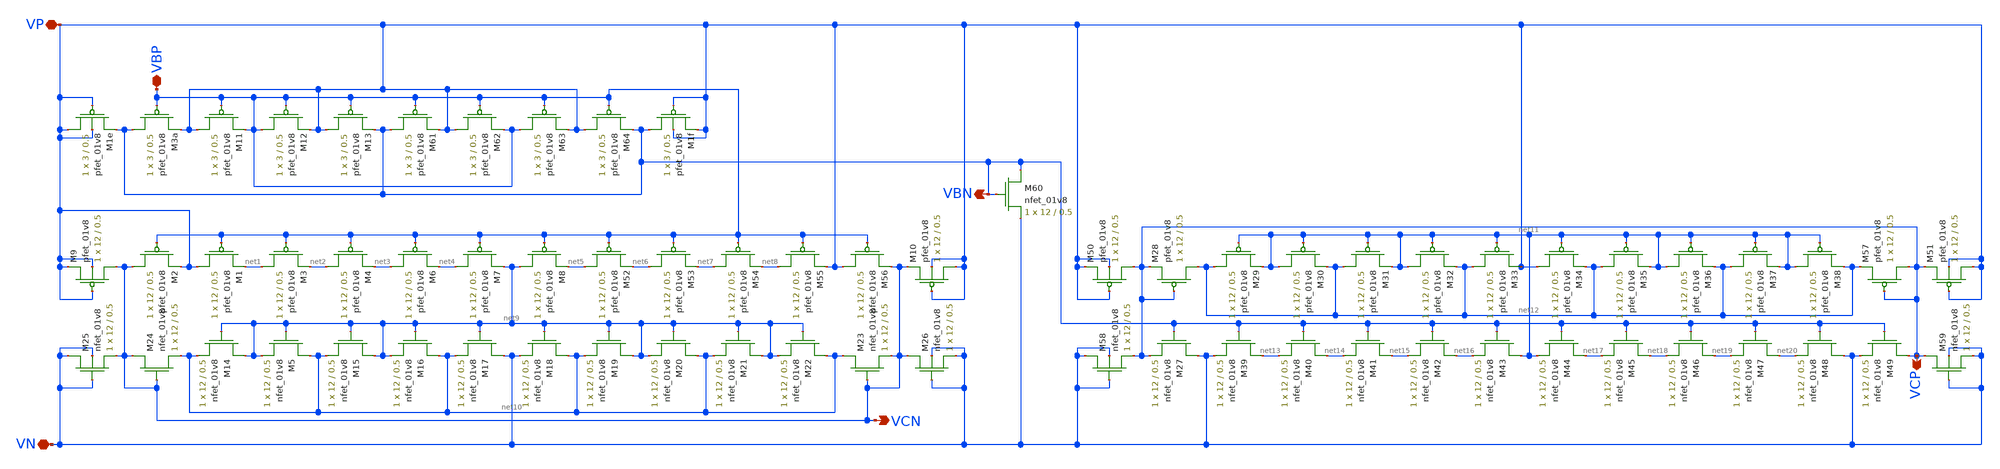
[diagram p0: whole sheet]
** sch_path: differential_amplifier/schematics/bias_generator.sch
**.subckt bias_generator VBP VP VN VCN VCP VBN
*.iopin VBP
*.iopin VP
*.iopin VN
*.opin VCN
*.opin VCP
*.opin VBN
XM9 VCN VP VP VP sky130_fd_pr__pfet_01v8 L=0.5 W=12 nf=1 ad='int((nf+1)/2) * W/nf * 0.29' as='int((nf+2)/2) * W/nf * 0.29'
+ pd='2*int((nf+1)/2) * (W/nf + 0.29)' ps='2*int((nf+2)/2) * (W/nf + 0.29)' nrd='0.29 / W' nrs='0.29 / W'
+ sa=0 sb=0 sd=0 mult=1 m=1
XM24 VCN VCN net10 VN sky130_fd_pr__nfet_01v8 L=0.5 W=12 nf=1 ad='int((nf+1)/2) * W/nf * 0.29' as='int((nf+2)/2) * W/nf * 0.29'
+ pd='2*int((nf+1)/2) * (W/nf + 0.29)' ps='2*int((nf+2)/2) * (W/nf + 0.29)' nrd='0.29 / W' nrs='0.29 / W'
+ sa=0 sb=0 sd=0 mult=1 m=1
XM2 VCN VBP VP VP sky130_fd_pr__pfet_01v8 L=0.5 W=12 nf=1 ad='int((nf+1)/2) * W/nf * 0.29' as='int((nf+2)/2) * W/nf * 0.29'
+ pd='2*int((nf+1)/2) * (W/nf + 0.29)' ps='2*int((nf+2)/2) * (W/nf + 0.29)' nrd='0.29 / W' nrs='0.29 / W'
+ sa=0 sb=0 sd=0 mult=1 m=1
XM10 VP VP VCN VP sky130_fd_pr__pfet_01v8 L=0.5 W=12 nf=1 ad='int((nf+1)/2) * W/nf * 0.29' as='int((nf+2)/2) * W/nf * 0.29'
+ pd='2*int((nf+1)/2) * (W/nf + 0.29)' ps='2*int((nf+2)/2) * (W/nf + 0.29)' nrd='0.29 / W' nrs='0.29 / W'
+ sa=0 sb=0 sd=0 mult=1 m=1
XM25 VN VN VCN VN sky130_fd_pr__nfet_01v8 L=0.5 W=12 nf=1 ad='int((nf+1)/2) * W/nf * 0.29' as='int((nf+2)/2) * W/nf * 0.29'
+ pd='2*int((nf+1)/2) * (W/nf + 0.29)' ps='2*int((nf+2)/2) * (W/nf + 0.29)' nrd='0.29 / W' nrs='0.29 / W'
+ sa=0 sb=0 sd=0 mult=1 m=1
XM26 VCN VN VN VN sky130_fd_pr__nfet_01v8 L=0.5 W=12 nf=1 ad='int((nf+1)/2) * W/nf * 0.29' as='int((nf+2)/2) * W/nf * 0.29'
+ pd='2*int((nf+1)/2) * (W/nf + 0.29)' ps='2*int((nf+2)/2) * (W/nf + 0.29)' nrd='0.29 / W' nrs='0.29 / W'
+ sa=0 sb=0 sd=0 mult=1 m=1
XM50 VCP VP VP VP sky130_fd_pr__pfet_01v8 L=0.5 W=12 nf=1 ad='int((nf+1)/2) * W/nf * 0.29' as='int((nf+2)/2) * W/nf * 0.29'
+ pd='2*int((nf+1)/2) * (W/nf + 0.29)' ps='2*int((nf+2)/2) * (W/nf + 0.29)' nrd='0.29 / W' nrs='0.29 / W'
+ sa=0 sb=0 sd=0 mult=1 m=1
XM51 VP VP VCP VP sky130_fd_pr__pfet_01v8 L=0.5 W=12 nf=1 ad='int((nf+1)/2) * W/nf * 0.29' as='int((nf+2)/2) * W/nf * 0.29'
+ pd='2*int((nf+1)/2) * (W/nf + 0.29)' ps='2*int((nf+2)/2) * (W/nf + 0.29)' nrd='0.29 / W' nrs='0.29 / W'
+ sa=0 sb=0 sd=0 mult=1 m=1
XM58 VN VN VCP VN sky130_fd_pr__nfet_01v8 L=0.5 W=12 nf=1 ad='int((nf+1)/2) * W/nf * 0.29' as='int((nf+2)/2) * W/nf * 0.29'
+ pd='2*int((nf+1)/2) * (W/nf + 0.29)' ps='2*int((nf+2)/2) * (W/nf + 0.29)' nrd='0.29 / W' nrs='0.29 / W'
+ sa=0 sb=0 sd=0 mult=1 m=1
XM59 VCP VN VN VN sky130_fd_pr__nfet_01v8 L=0.5 W=12 nf=1 ad='int((nf+1)/2) * W/nf * 0.29' as='int((nf+2)/2) * W/nf * 0.29'
+ pd='2*int((nf+1)/2) * (W/nf + 0.29)' ps='2*int((nf+2)/2) * (W/nf + 0.29)' nrd='0.29 / W' nrs='0.29 / W'
+ sa=0 sb=0 sd=0 mult=1 m=1
XM3a VBN VBP VP VP sky130_fd_pr__pfet_01v8 L=0.5 W=3 nf=1 ad='int((nf+1)/2) * W/nf * 0.29' as='int((nf+2)/2) * W/nf * 0.29'
+ pd='2*int((nf+1)/2) * (W/nf + 0.29)' ps='2*int((nf+2)/2) * (W/nf + 0.29)' nrd='0.29 / W' nrs='0.29 / W'
+ sa=0 sb=0 sd=0 mult=1 m=1
XM1e VP VP VBN VP sky130_fd_pr__pfet_01v8 L=0.5 W=3 nf=1 ad='int((nf+1)/2) * W/nf * 0.29' as='int((nf+2)/2) * W/nf * 0.29'
+ pd='2*int((nf+1)/2) * (W/nf + 0.29)' ps='2*int((nf+2)/2) * (W/nf + 0.29)' nrd='0.29 / W' nrs='0.29 / W'
+ sa=0 sb=0 sd=0 mult=1 m=1
XM1f VBN VP VP VP sky130_fd_pr__pfet_01v8 L=0.5 W=3 nf=1 ad='int((nf+1)/2) * W/nf * 0.29' as='int((nf+2)/2) * W/nf * 0.29'
+ pd='2*int((nf+1)/2) * (W/nf + 0.29)' ps='2*int((nf+2)/2) * (W/nf + 0.29)' nrd='0.29 / W' nrs='0.29 / W'
+ sa=0 sb=0 sd=0 mult=1 m=1
XM60 VBN VBN VN VN sky130_fd_pr__nfet_01v8 L=0.5 W=12 nf=1 ad='int((nf+1)/2) * W/nf * 0.29' as='int((nf+2)/2) * W/nf * 0.29'
+ pd='2*int((nf+1)/2) * (W/nf + 0.29)' ps='2*int((nf+2)/2) * (W/nf + 0.29)' nrd='0.29 / W' nrs='0.29 / W'
+ sa=0 sb=0 sd=0 mult=1 m=1
XM11 VP VBP VBP VP sky130_fd_pr__pfet_01v8 L=0.5 W=3 nf=1 ad='int((nf+1)/2) * W/nf * 0.29' as='int((nf+2)/2) * W/nf * 0.29'
+ pd='2*int((nf+1)/2) * (W/nf + 0.29)' ps='2*int((nf+2)/2) * (W/nf + 0.29)' nrd='0.29 / W' nrs='0.29 / W'
+ sa=0 sb=0 sd=0 mult=1 m=1
XM12 VBP VBP VP VP sky130_fd_pr__pfet_01v8 L=0.5 W=3 nf=1 ad='int((nf+1)/2) * W/nf * 0.29' as='int((nf+2)/2) * W/nf * 0.29'
+ pd='2*int((nf+1)/2) * (W/nf + 0.29)' ps='2*int((nf+2)/2) * (W/nf + 0.29)' nrd='0.29 / W' nrs='0.29 / W'
+ sa=0 sb=0 sd=0 mult=1 m=1
XM13 VP VBP VBN VP sky130_fd_pr__pfet_01v8 L=0.5 W=3 nf=1 ad='int((nf+1)/2) * W/nf * 0.29' as='int((nf+2)/2) * W/nf * 0.29'
+ pd='2*int((nf+1)/2) * (W/nf + 0.29)' ps='2*int((nf+2)/2) * (W/nf + 0.29)' nrd='0.29 / W' nrs='0.29 / W'
+ sa=0 sb=0 sd=0 mult=1 m=1
XM61 VBN VBP VP VP sky130_fd_pr__pfet_01v8 L=0.5 W=3 nf=1 ad='int((nf+1)/2) * W/nf * 0.29' as='int((nf+2)/2) * W/nf * 0.29'
+ pd='2*int((nf+1)/2) * (W/nf + 0.29)' ps='2*int((nf+2)/2) * (W/nf + 0.29)' nrd='0.29 / W' nrs='0.29 / W'
+ sa=0 sb=0 sd=0 mult=1 m=1
XM62 VP VBP VBP VP sky130_fd_pr__pfet_01v8 L=0.5 W=3 nf=1 ad='int((nf+1)/2) * W/nf * 0.29' as='int((nf+2)/2) * W/nf * 0.29'
+ pd='2*int((nf+1)/2) * (W/nf + 0.29)' ps='2*int((nf+2)/2) * (W/nf + 0.29)' nrd='0.29 / W' nrs='0.29 / W'
+ sa=0 sb=0 sd=0 mult=1 m=1
XM63 VBP VBP VP VP sky130_fd_pr__pfet_01v8 L=0.5 W=3 nf=1 ad='int((nf+1)/2) * W/nf * 0.29' as='int((nf+2)/2) * W/nf * 0.29'
+ pd='2*int((nf+1)/2) * (W/nf + 0.29)' ps='2*int((nf+2)/2) * (W/nf + 0.29)' nrd='0.29 / W' nrs='0.29 / W'
+ sa=0 sb=0 sd=0 mult=1 m=1
XM64 VP VBP VBN VP sky130_fd_pr__pfet_01v8 L=0.5 W=3 nf=1 ad='int((nf+1)/2) * W/nf * 0.29' as='int((nf+2)/2) * W/nf * 0.29'
+ pd='2*int((nf+1)/2) * (W/nf + 0.29)' ps='2*int((nf+2)/2) * (W/nf + 0.29)' nrd='0.29 / W' nrs='0.29 / W'
+ sa=0 sb=0 sd=0 mult=1 m=1
XM1 VP VBP net1 VP sky130_fd_pr__pfet_01v8 L=0.5 W=12 nf=1 ad='int((nf+1)/2) * W/nf * 0.29' as='int((nf+2)/2) * W/nf * 0.29'
+ pd='2*int((nf+1)/2) * (W/nf + 0.29)' ps='2*int((nf+2)/2) * (W/nf + 0.29)' nrd='0.29 / W' nrs='0.29 / W'
+ sa=0 sb=0 sd=0 mult=1 m=1
XM3 net1 VBP net2 VP sky130_fd_pr__pfet_01v8 L=0.5 W=12 nf=1 ad='int((nf+1)/2) * W/nf * 0.29' as='int((nf+2)/2) * W/nf * 0.29'
+ pd='2*int((nf+1)/2) * (W/nf + 0.29)' ps='2*int((nf+2)/2) * (W/nf + 0.29)' nrd='0.29 / W' nrs='0.29 / W'
+ sa=0 sb=0 sd=0 mult=1 m=1
XM4 net2 VBP net3 VP sky130_fd_pr__pfet_01v8 L=0.5 W=12 nf=1 ad='int((nf+1)/2) * W/nf * 0.29' as='int((nf+2)/2) * W/nf * 0.29'
+ pd='2*int((nf+1)/2) * (W/nf + 0.29)' ps='2*int((nf+2)/2) * (W/nf + 0.29)' nrd='0.29 / W' nrs='0.29 / W'
+ sa=0 sb=0 sd=0 mult=1 m=1
XM6 net3 VBP net4 VP sky130_fd_pr__pfet_01v8 L=0.5 W=12 nf=1 ad='int((nf+1)/2) * W/nf * 0.29' as='int((nf+2)/2) * W/nf * 0.29'
+ pd='2*int((nf+1)/2) * (W/nf + 0.29)' ps='2*int((nf+2)/2) * (W/nf + 0.29)' nrd='0.29 / W' nrs='0.29 / W'
+ sa=0 sb=0 sd=0 mult=1 m=1
XM7 net4 VBP net9 VP sky130_fd_pr__pfet_01v8 L=0.5 W=12 nf=1 ad='int((nf+1)/2) * W/nf * 0.29' as='int((nf+2)/2) * W/nf * 0.29'
+ pd='2*int((nf+1)/2) * (W/nf + 0.29)' ps='2*int((nf+2)/2) * (W/nf + 0.29)' nrd='0.29 / W' nrs='0.29 / W'
+ sa=0 sb=0 sd=0 mult=1 m=1
XM8 net9 VBP net5 VP sky130_fd_pr__pfet_01v8 L=0.5 W=12 nf=1 ad='int((nf+1)/2) * W/nf * 0.29' as='int((nf+2)/2) * W/nf * 0.29'
+ pd='2*int((nf+1)/2) * (W/nf + 0.29)' ps='2*int((nf+2)/2) * (W/nf + 0.29)' nrd='0.29 / W' nrs='0.29 / W'
+ sa=0 sb=0 sd=0 mult=1 m=1
XM52 net5 VBP net6 VP sky130_fd_pr__pfet_01v8 L=0.5 W=12 nf=1 ad='int((nf+1)/2) * W/nf * 0.29' as='int((nf+2)/2) * W/nf * 0.29'
+ pd='2*int((nf+1)/2) * (W/nf + 0.29)' ps='2*int((nf+2)/2) * (W/nf + 0.29)' nrd='0.29 / W' nrs='0.29 / W'
+ sa=0 sb=0 sd=0 mult=1 m=1
XM53 net6 VBP net7 VP sky130_fd_pr__pfet_01v8 L=0.5 W=12 nf=1 ad='int((nf+1)/2) * W/nf * 0.29' as='int((nf+2)/2) * W/nf * 0.29'
+ pd='2*int((nf+1)/2) * (W/nf + 0.29)' ps='2*int((nf+2)/2) * (W/nf + 0.29)' nrd='0.29 / W' nrs='0.29 / W'
+ sa=0 sb=0 sd=0 mult=1 m=1
XM54 net7 VBP net8 VP sky130_fd_pr__pfet_01v8 L=0.5 W=12 nf=1 ad='int((nf+1)/2) * W/nf * 0.29' as='int((nf+2)/2) * W/nf * 0.29'
+ pd='2*int((nf+1)/2) * (W/nf + 0.29)' ps='2*int((nf+2)/2) * (W/nf + 0.29)' nrd='0.29 / W' nrs='0.29 / W'
+ sa=0 sb=0 sd=0 mult=1 m=1
XM55 net8 VBP VP VP sky130_fd_pr__pfet_01v8 L=0.5 W=12 nf=1 ad='int((nf+1)/2) * W/nf * 0.29' as='int((nf+2)/2) * W/nf * 0.29'
+ pd='2*int((nf+1)/2) * (W/nf + 0.29)' ps='2*int((nf+2)/2) * (W/nf + 0.29)' nrd='0.29 / W' nrs='0.29 / W'
+ sa=0 sb=0 sd=0 mult=1 m=1
XM56 VP VBP VCN VP sky130_fd_pr__pfet_01v8 L=0.5 W=12 nf=1 ad='int((nf+1)/2) * W/nf * 0.29' as='int((nf+2)/2) * W/nf * 0.29'
+ pd='2*int((nf+1)/2) * (W/nf + 0.29)' ps='2*int((nf+2)/2) * (W/nf + 0.29)' nrd='0.29 / W' nrs='0.29 / W'
+ sa=0 sb=0 sd=0 mult=1 m=1
XM14 net9 net9 net10 VN sky130_fd_pr__nfet_01v8 L=0.5 W=12 nf=1 ad='int((nf+1)/2) * W/nf * 0.29' as='int((nf+2)/2) * W/nf * 0.29'
+ pd='2*int((nf+1)/2) * (W/nf + 0.29)' ps='2*int((nf+2)/2) * (W/nf + 0.29)' nrd='0.29 / W' nrs='0.29 / W'
+ sa=0 sb=0 sd=0 mult=1 m=1
XM5 net10 net9 net9 VN sky130_fd_pr__nfet_01v8 L=0.5 W=12 nf=1 ad='int((nf+1)/2) * W/nf * 0.29' as='int((nf+2)/2) * W/nf * 0.29'
+ pd='2*int((nf+1)/2) * (W/nf + 0.29)' ps='2*int((nf+2)/2) * (W/nf + 0.29)' nrd='0.29 / W' nrs='0.29 / W'
+ sa=0 sb=0 sd=0 mult=1 m=1
XM15 net9 net9 net10 VN sky130_fd_pr__nfet_01v8 L=0.5 W=12 nf=1 ad='int((nf+1)/2) * W/nf * 0.29' as='int((nf+2)/2) * W/nf * 0.29'
+ pd='2*int((nf+1)/2) * (W/nf + 0.29)' ps='2*int((nf+2)/2) * (W/nf + 0.29)' nrd='0.29 / W' nrs='0.29 / W'
+ sa=0 sb=0 sd=0 mult=1 m=1
XM16 net10 net9 net9 VN sky130_fd_pr__nfet_01v8 L=0.5 W=12 nf=1 ad='int((nf+1)/2) * W/nf * 0.29' as='int((nf+2)/2) * W/nf * 0.29'
+ pd='2*int((nf+1)/2) * (W/nf + 0.29)' ps='2*int((nf+2)/2) * (W/nf + 0.29)' nrd='0.29 / W' nrs='0.29 / W'
+ sa=0 sb=0 sd=0 mult=1 m=1
XM17 VN net9 net10 VN sky130_fd_pr__nfet_01v8 L=0.5 W=12 nf=1 ad='int((nf+1)/2) * W/nf * 0.29' as='int((nf+2)/2) * W/nf * 0.29'
+ pd='2*int((nf+1)/2) * (W/nf + 0.29)' ps='2*int((nf+2)/2) * (W/nf + 0.29)' nrd='0.29 / W' nrs='0.29 / W'
+ sa=0 sb=0 sd=0 mult=1 m=1
XM18 net10 net9 VN VN sky130_fd_pr__nfet_01v8 L=0.5 W=12 nf=1 ad='int((nf+1)/2) * W/nf * 0.29' as='int((nf+2)/2) * W/nf * 0.29'
+ pd='2*int((nf+1)/2) * (W/nf + 0.29)' ps='2*int((nf+2)/2) * (W/nf + 0.29)' nrd='0.29 / W' nrs='0.29 / W'
+ sa=0 sb=0 sd=0 mult=1 m=1
XM19 net9 net9 net10 VN sky130_fd_pr__nfet_01v8 L=0.5 W=12 nf=1 ad='int((nf+1)/2) * W/nf * 0.29' as='int((nf+2)/2) * W/nf * 0.29'
+ pd='2*int((nf+1)/2) * (W/nf + 0.29)' ps='2*int((nf+2)/2) * (W/nf + 0.29)' nrd='0.29 / W' nrs='0.29 / W'
+ sa=0 sb=0 sd=0 mult=1 m=1
XM20 net10 net9 net9 VN sky130_fd_pr__nfet_01v8 L=0.5 W=12 nf=1 ad='int((nf+1)/2) * W/nf * 0.29' as='int((nf+2)/2) * W/nf * 0.29'
+ pd='2*int((nf+1)/2) * (W/nf + 0.29)' ps='2*int((nf+2)/2) * (W/nf + 0.29)' nrd='0.29 / W' nrs='0.29 / W'
+ sa=0 sb=0 sd=0 mult=1 m=1
XM21 net9 net9 net10 VN sky130_fd_pr__nfet_01v8 L=0.5 W=12 nf=1 ad='int((nf+1)/2) * W/nf * 0.29' as='int((nf+2)/2) * W/nf * 0.29'
+ pd='2*int((nf+1)/2) * (W/nf + 0.29)' ps='2*int((nf+2)/2) * (W/nf + 0.29)' nrd='0.29 / W' nrs='0.29 / W'
+ sa=0 sb=0 sd=0 mult=1 m=1
XM22 net10 net9 net9 VN sky130_fd_pr__nfet_01v8 L=0.5 W=12 nf=1 ad='int((nf+1)/2) * W/nf * 0.29' as='int((nf+2)/2) * W/nf * 0.29'
+ pd='2*int((nf+1)/2) * (W/nf + 0.29)' ps='2*int((nf+2)/2) * (W/nf + 0.29)' nrd='0.29 / W' nrs='0.29 / W'
+ sa=0 sb=0 sd=0 mult=1 m=1
XM23 net10 VCN VCN VN sky130_fd_pr__nfet_01v8 L=0.5 W=12 nf=1 ad='int((nf+1)/2) * W/nf * 0.29' as='int((nf+2)/2) * W/nf * 0.29'
+ pd='2*int((nf+1)/2) * (W/nf + 0.29)' ps='2*int((nf+2)/2) * (W/nf + 0.29)' nrd='0.29 / W' nrs='0.29 / W'
+ sa=0 sb=0 sd=0 mult=1 m=1
XM28 net12 VCP VCP VP sky130_fd_pr__pfet_01v8 L=0.5 W=12 nf=1 ad='int((nf+1)/2) * W/nf * 0.29' as='int((nf+2)/2) * W/nf * 0.29'
+ pd='2*int((nf+1)/2) * (W/nf + 0.29)' ps='2*int((nf+2)/2) * (W/nf + 0.29)' nrd='0.29 / W' nrs='0.29 / W'
+ sa=0 sb=0 sd=0 mult=1 m=1
XM29 net12 net11 net11 VP sky130_fd_pr__pfet_01v8 L=0.5 W=12 nf=1 ad='int((nf+1)/2) * W/nf * 0.29' as='int((nf+2)/2) * W/nf * 0.29'
+ pd='2*int((nf+1)/2) * (W/nf + 0.29)' ps='2*int((nf+2)/2) * (W/nf + 0.29)' nrd='0.29 / W' nrs='0.29 / W'
+ sa=0 sb=0 sd=0 mult=1 m=1
XM30 net11 net11 net12 VP sky130_fd_pr__pfet_01v8 L=0.5 W=12 nf=1 ad='int((nf+1)/2) * W/nf * 0.29' as='int((nf+2)/2) * W/nf * 0.29'
+ pd='2*int((nf+1)/2) * (W/nf + 0.29)' ps='2*int((nf+2)/2) * (W/nf + 0.29)' nrd='0.29 / W' nrs='0.29 / W'
+ sa=0 sb=0 sd=0 mult=1 m=1
XM31 net12 net11 net11 VP sky130_fd_pr__pfet_01v8 L=0.5 W=12 nf=1 ad='int((nf+1)/2) * W/nf * 0.29' as='int((nf+2)/2) * W/nf * 0.29'
+ pd='2*int((nf+1)/2) * (W/nf + 0.29)' ps='2*int((nf+2)/2) * (W/nf + 0.29)' nrd='0.29 / W' nrs='0.29 / W'
+ sa=0 sb=0 sd=0 mult=1 m=1
XM32 net11 net11 net12 VP sky130_fd_pr__pfet_01v8 L=0.5 W=12 nf=1 ad='int((nf+1)/2) * W/nf * 0.29' as='int((nf+2)/2) * W/nf * 0.29'
+ pd='2*int((nf+1)/2) * (W/nf + 0.29)' ps='2*int((nf+2)/2) * (W/nf + 0.29)' nrd='0.29 / W' nrs='0.29 / W'
+ sa=0 sb=0 sd=0 mult=1 m=1
XM33 net12 net11 VP VP sky130_fd_pr__pfet_01v8 L=0.5 W=12 nf=1 ad='int((nf+1)/2) * W/nf * 0.29' as='int((nf+2)/2) * W/nf * 0.29'
+ pd='2*int((nf+1)/2) * (W/nf + 0.29)' ps='2*int((nf+2)/2) * (W/nf + 0.29)' nrd='0.29 / W' nrs='0.29 / W'
+ sa=0 sb=0 sd=0 mult=1 m=1
XM34 VP net11 net12 VP sky130_fd_pr__pfet_01v8 L=0.5 W=12 nf=1 ad='int((nf+1)/2) * W/nf * 0.29' as='int((nf+2)/2) * W/nf * 0.29'
+ pd='2*int((nf+1)/2) * (W/nf + 0.29)' ps='2*int((nf+2)/2) * (W/nf + 0.29)' nrd='0.29 / W' nrs='0.29 / W'
+ sa=0 sb=0 sd=0 mult=1 m=1
XM35 net12 net11 net11 VP sky130_fd_pr__pfet_01v8 L=0.5 W=12 nf=1 ad='int((nf+1)/2) * W/nf * 0.29' as='int((nf+2)/2) * W/nf * 0.29'
+ pd='2*int((nf+1)/2) * (W/nf + 0.29)' ps='2*int((nf+2)/2) * (W/nf + 0.29)' nrd='0.29 / W' nrs='0.29 / W'
+ sa=0 sb=0 sd=0 mult=1 m=1
XM36 net11 net11 net12 VP sky130_fd_pr__pfet_01v8 L=0.5 W=12 nf=1 ad='int((nf+1)/2) * W/nf * 0.29' as='int((nf+2)/2) * W/nf * 0.29'
+ pd='2*int((nf+1)/2) * (W/nf + 0.29)' ps='2*int((nf+2)/2) * (W/nf + 0.29)' nrd='0.29 / W' nrs='0.29 / W'
+ sa=0 sb=0 sd=0 mult=1 m=1
XM37 net12 net11 net11 VP sky130_fd_pr__pfet_01v8 L=0.5 W=12 nf=1 ad='int((nf+1)/2) * W/nf * 0.29' as='int((nf+2)/2) * W/nf * 0.29'
+ pd='2*int((nf+1)/2) * (W/nf + 0.29)' ps='2*int((nf+2)/2) * (W/nf + 0.29)' nrd='0.29 / W' nrs='0.29 / W'
+ sa=0 sb=0 sd=0 mult=1 m=1
XM38 net11 net11 net12 VP sky130_fd_pr__pfet_01v8 L=0.5 W=12 nf=1 ad='int((nf+1)/2) * W/nf * 0.29' as='int((nf+2)/2) * W/nf * 0.29'
+ pd='2*int((nf+1)/2) * (W/nf + 0.29)' ps='2*int((nf+2)/2) * (W/nf + 0.29)' nrd='0.29 / W' nrs='0.29 / W'
+ sa=0 sb=0 sd=0 mult=1 m=1
XM57 VCP VCP net12 VP sky130_fd_pr__pfet_01v8 L=0.5 W=12 nf=1 ad='int((nf+1)/2) * W/nf * 0.29' as='int((nf+2)/2) * W/nf * 0.29'
+ pd='2*int((nf+1)/2) * (W/nf + 0.29)' ps='2*int((nf+2)/2) * (W/nf + 0.29)' nrd='0.29 / W' nrs='0.29 / W'
+ sa=0 sb=0 sd=0 mult=1 m=1
XM27 VN VBN VCP VN sky130_fd_pr__nfet_01v8 L=0.5 W=12 nf=1 ad='int((nf+1)/2) * W/nf * 0.29' as='int((nf+2)/2) * W/nf * 0.29'
+ pd='2*int((nf+1)/2) * (W/nf + 0.29)' ps='2*int((nf+2)/2) * (W/nf + 0.29)' nrd='0.29 / W' nrs='0.29 / W'
+ sa=0 sb=0 sd=0 mult=1 m=1
XM39 net13 VBN VN VN sky130_fd_pr__nfet_01v8 L=0.5 W=12 nf=1 ad='int((nf+1)/2) * W/nf * 0.29' as='int((nf+2)/2) * W/nf * 0.29'
+ pd='2*int((nf+1)/2) * (W/nf + 0.29)' ps='2*int((nf+2)/2) * (W/nf + 0.29)' nrd='0.29 / W' nrs='0.29 / W'
+ sa=0 sb=0 sd=0 mult=1 m=1
XM40 net14 VBN net13 VN sky130_fd_pr__nfet_01v8 L=0.5 W=12 nf=1 ad='int((nf+1)/2) * W/nf * 0.29' as='int((nf+2)/2) * W/nf * 0.29'
+ pd='2*int((nf+1)/2) * (W/nf + 0.29)' ps='2*int((nf+2)/2) * (W/nf + 0.29)' nrd='0.29 / W' nrs='0.29 / W'
+ sa=0 sb=0 sd=0 mult=1 m=1
XM41 net15 VBN net14 VN sky130_fd_pr__nfet_01v8 L=0.5 W=12 nf=1 ad='int((nf+1)/2) * W/nf * 0.29' as='int((nf+2)/2) * W/nf * 0.29'
+ pd='2*int((nf+1)/2) * (W/nf + 0.29)' ps='2*int((nf+2)/2) * (W/nf + 0.29)' nrd='0.29 / W' nrs='0.29 / W'
+ sa=0 sb=0 sd=0 mult=1 m=1
XM42 net16 VBN net15 VN sky130_fd_pr__nfet_01v8 L=0.5 W=12 nf=1 ad='int((nf+1)/2) * W/nf * 0.29' as='int((nf+2)/2) * W/nf * 0.29'
+ pd='2*int((nf+1)/2) * (W/nf + 0.29)' ps='2*int((nf+2)/2) * (W/nf + 0.29)' nrd='0.29 / W' nrs='0.29 / W'
+ sa=0 sb=0 sd=0 mult=1 m=1
XM43 net11 VBN net16 VN sky130_fd_pr__nfet_01v8 L=0.5 W=12 nf=1 ad='int((nf+1)/2) * W/nf * 0.29' as='int((nf+2)/2) * W/nf * 0.29'
+ pd='2*int((nf+1)/2) * (W/nf + 0.29)' ps='2*int((nf+2)/2) * (W/nf + 0.29)' nrd='0.29 / W' nrs='0.29 / W'
+ sa=0 sb=0 sd=0 mult=1 m=1
XM44 net17 VBN net11 VN sky130_fd_pr__nfet_01v8 L=0.5 W=12 nf=1 ad='int((nf+1)/2) * W/nf * 0.29' as='int((nf+2)/2) * W/nf * 0.29'
+ pd='2*int((nf+1)/2) * (W/nf + 0.29)' ps='2*int((nf+2)/2) * (W/nf + 0.29)' nrd='0.29 / W' nrs='0.29 / W'
+ sa=0 sb=0 sd=0 mult=1 m=1
XM45 net18 VBN net17 VN sky130_fd_pr__nfet_01v8 L=0.5 W=12 nf=1 ad='int((nf+1)/2) * W/nf * 0.29' as='int((nf+2)/2) * W/nf * 0.29'
+ pd='2*int((nf+1)/2) * (W/nf + 0.29)' ps='2*int((nf+2)/2) * (W/nf + 0.29)' nrd='0.29 / W' nrs='0.29 / W'
+ sa=0 sb=0 sd=0 mult=1 m=1
XM46 net19 VBN net18 VN sky130_fd_pr__nfet_01v8 L=0.5 W=12 nf=1 ad='int((nf+1)/2) * W/nf * 0.29' as='int((nf+2)/2) * W/nf * 0.29'
+ pd='2*int((nf+1)/2) * (W/nf + 0.29)' ps='2*int((nf+2)/2) * (W/nf + 0.29)' nrd='0.29 / W' nrs='0.29 / W'
+ sa=0 sb=0 sd=0 mult=1 m=1
XM47 net20 VBN net19 VN sky130_fd_pr__nfet_01v8 L=0.5 W=12 nf=1 ad='int((nf+1)/2) * W/nf * 0.29' as='int((nf+2)/2) * W/nf * 0.29'
+ pd='2*int((nf+1)/2) * (W/nf + 0.29)' ps='2*int((nf+2)/2) * (W/nf + 0.29)' nrd='0.29 / W' nrs='0.29 / W'
+ sa=0 sb=0 sd=0 mult=1 m=1
XM48 VN VBN net20 VN sky130_fd_pr__nfet_01v8 L=0.5 W=12 nf=1 ad='int((nf+1)/2) * W/nf * 0.29' as='int((nf+2)/2) * W/nf * 0.29'
+ pd='2*int((nf+1)/2) * (W/nf + 0.29)' ps='2*int((nf+2)/2) * (W/nf + 0.29)' nrd='0.29 / W' nrs='0.29 / W'
+ sa=0 sb=0 sd=0 mult=1 m=1
XM49 VCP VBN VN VN sky130_fd_pr__nfet_01v8 L=0.5 W=12 nf=1 ad='int((nf+1)/2) * W/nf * 0.29' as='int((nf+2)/2) * W/nf * 0.29'
+ pd='2*int((nf+1)/2) * (W/nf + 0.29)' ps='2*int((nf+2)/2) * (W/nf + 0.29)' nrd='0.29 / W' nrs='0.29 / W'
+ sa=0 sb=0 sd=0 mult=1 m=1
**.ends
.end
